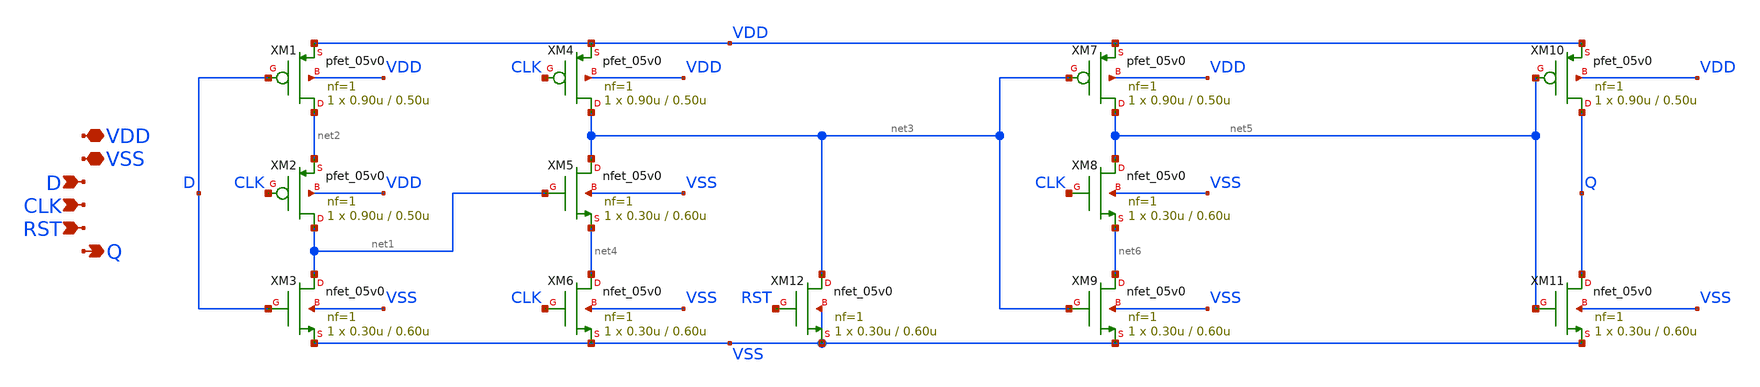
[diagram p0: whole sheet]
** sch_path: designs/libs/core_analog/digital/digital_dff_tspc.sch
**.subckt digital_dff_tspc VDD VSS D CLK Q RST
*.iopin VDD
*.iopin VSS
*.ipin D
*.ipin CLK
*.opin Q
*.ipin RST
XM1 net2 D VDD VDD pfet_05v0 L=0.50u W=0.90u nf=1 ad='int((nf+1)/2) * W/nf * 0.18u' as='int((nf+2)/2) * W/nf * 0.18u'
+ pd='2*int((nf+1)/2) * (W/nf + 0.18u)' ps='2*int((nf+2)/2) * (W/nf + 0.18u)' nrd='0.18u / W' nrs='0.18u / W'
+ sa=0 sb=0 sd=0 m=1
XM2 net1 CLK net2 VDD pfet_05v0 L=0.50u W=0.90u nf=1 ad='int((nf+1)/2) * W/nf * 0.18u' as='int((nf+2)/2) * W/nf * 0.18u'
+ pd='2*int((nf+1)/2) * (W/nf + 0.18u)' ps='2*int((nf+2)/2) * (W/nf + 0.18u)' nrd='0.18u / W' nrs='0.18u / W'
+ sa=0 sb=0 sd=0 m=1
XM3 net1 D VSS VSS nfet_05v0 L=0.60u W=0.30u nf=1 ad='int((nf+1)/2) * W/nf * 0.18u' as='int((nf+2)/2) * W/nf * 0.18u'
+ pd='2*int((nf+1)/2) * (W/nf + 0.18u)' ps='2*int((nf+2)/2) * (W/nf + 0.18u)' nrd='0.18u / W' nrs='0.18u / W'
+ sa=0 sb=0 sd=0 m=1
XM4 net3 CLK VDD VDD pfet_05v0 L=0.50u W=0.90u nf=1 ad='int((nf+1)/2) * W/nf * 0.18u' as='int((nf+2)/2) * W/nf * 0.18u'
+ pd='2*int((nf+1)/2) * (W/nf + 0.18u)' ps='2*int((nf+2)/2) * (W/nf + 0.18u)' nrd='0.18u / W' nrs='0.18u / W'
+ sa=0 sb=0 sd=0 m=1
XM5 net3 net1 net4 VSS nfet_05v0 L=0.60u W=0.30u nf=1 ad='int((nf+1)/2) * W/nf * 0.18u' as='int((nf+2)/2) * W/nf * 0.18u'
+ pd='2*int((nf+1)/2) * (W/nf + 0.18u)' ps='2*int((nf+2)/2) * (W/nf + 0.18u)' nrd='0.18u / W' nrs='0.18u / W'
+ sa=0 sb=0 sd=0 m=1
XM6 net4 CLK VSS VSS nfet_05v0 L=0.60u W=0.30u nf=1 ad='int((nf+1)/2) * W/nf * 0.18u' as='int((nf+2)/2) * W/nf * 0.18u'
+ pd='2*int((nf+1)/2) * (W/nf + 0.18u)' ps='2*int((nf+2)/2) * (W/nf + 0.18u)' nrd='0.18u / W' nrs='0.18u / W'
+ sa=0 sb=0 sd=0 m=1
XM7 net5 net3 VDD VDD pfet_05v0 L=0.50u W=0.90u nf=1 ad='int((nf+1)/2) * W/nf * 0.18u' as='int((nf+2)/2) * W/nf * 0.18u'
+ pd='2*int((nf+1)/2) * (W/nf + 0.18u)' ps='2*int((nf+2)/2) * (W/nf + 0.18u)' nrd='0.18u / W' nrs='0.18u / W'
+ sa=0 sb=0 sd=0 m=1
XM8 net5 CLK net6 VSS nfet_05v0 L=0.60u W=0.30u nf=1 ad='int((nf+1)/2) * W/nf * 0.18u' as='int((nf+2)/2) * W/nf * 0.18u'
+ pd='2*int((nf+1)/2) * (W/nf + 0.18u)' ps='2*int((nf+2)/2) * (W/nf + 0.18u)' nrd='0.18u / W' nrs='0.18u / W'
+ sa=0 sb=0 sd=0 m=1
XM9 net6 net3 VSS VSS nfet_05v0 L=0.60u W=0.30u nf=1 ad='int((nf+1)/2) * W/nf * 0.18u' as='int((nf+2)/2) * W/nf * 0.18u'
+ pd='2*int((nf+1)/2) * (W/nf + 0.18u)' ps='2*int((nf+2)/2) * (W/nf + 0.18u)' nrd='0.18u / W' nrs='0.18u / W'
+ sa=0 sb=0 sd=0 m=1
XM10 Q net5 VDD VDD pfet_05v0 L=0.50u W=0.90u nf=1 ad='int((nf+1)/2) * W/nf * 0.18u' as='int((nf+2)/2) * W/nf * 0.18u'
+ pd='2*int((nf+1)/2) * (W/nf + 0.18u)' ps='2*int((nf+2)/2) * (W/nf + 0.18u)' nrd='0.18u / W' nrs='0.18u / W'
+ sa=0 sb=0 sd=0 m=1
XM11 Q net5 VSS VSS nfet_05v0 L=0.60u W=0.30u nf=1 ad='int((nf+1)/2) * W/nf * 0.18u' as='int((nf+2)/2) * W/nf * 0.18u'
+ pd='2*int((nf+1)/2) * (W/nf + 0.18u)' ps='2*int((nf+2)/2) * (W/nf + 0.18u)' nrd='0.18u / W' nrs='0.18u / W'
+ sa=0 sb=0 sd=0 m=1
XM12 net3 RST VSS VSS nfet_05v0 L=0.60u W=0.30u nf=1 ad='int((nf+1)/2) * W/nf * 0.18u' as='int((nf+2)/2) * W/nf * 0.18u'
+ pd='2*int((nf+1)/2) * (W/nf + 0.18u)' ps='2*int((nf+2)/2) * (W/nf + 0.18u)' nrd='0.18u / W' nrs='0.18u / W'
+ sa=0 sb=0 sd=0 m=1
**.ends
.end
